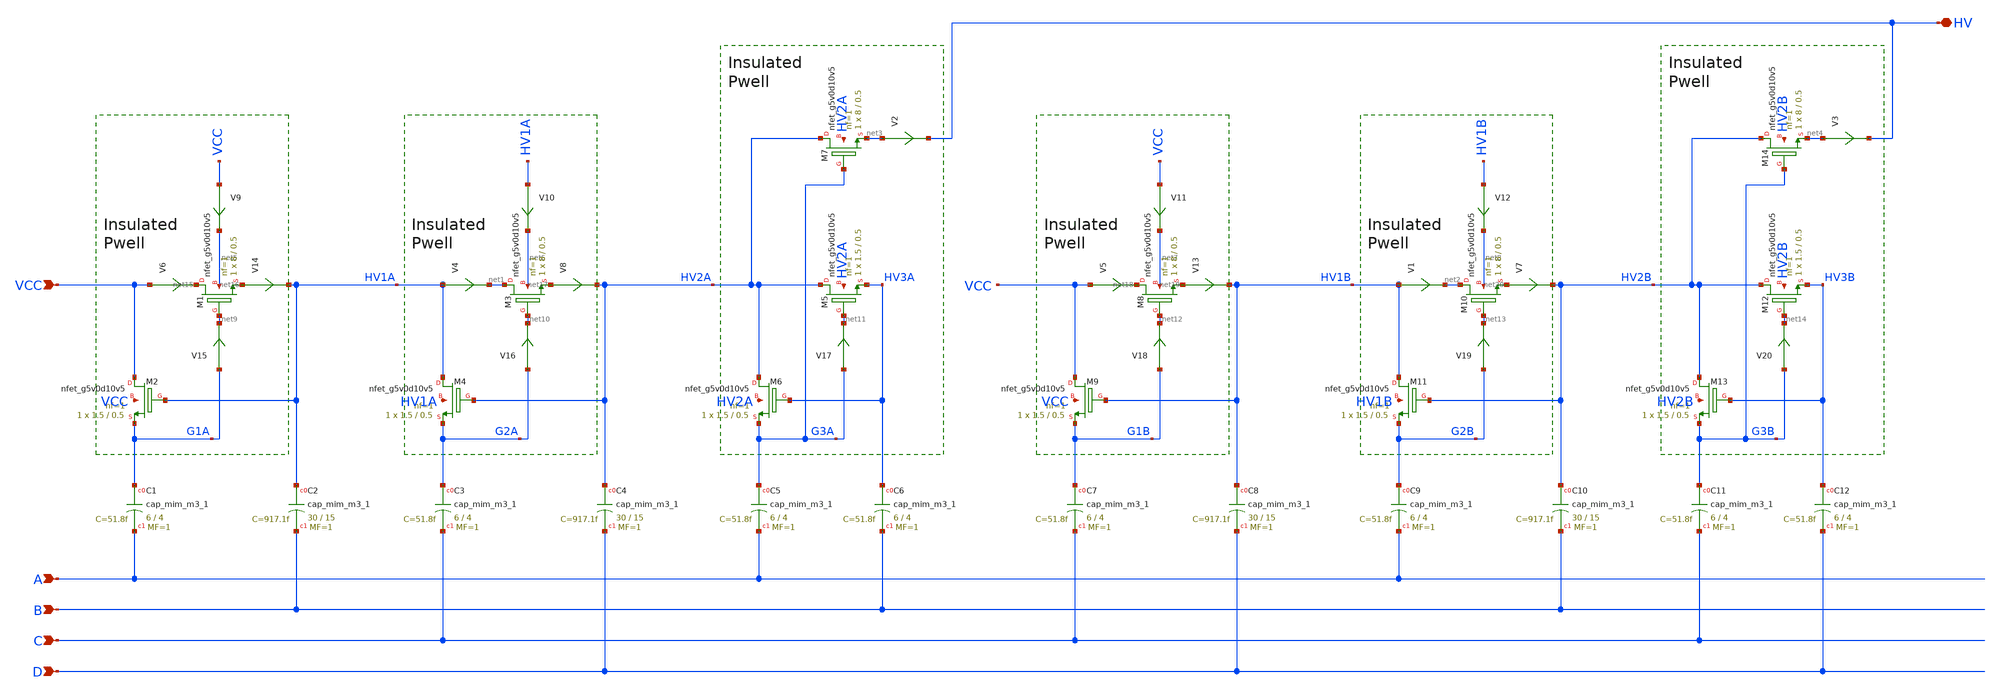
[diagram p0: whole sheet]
** sch_path: sky130A/xschem_libs/sky130_tests_ase/charge_pump/schematic/charge_pump.sch
* Copyright 2021 Stefan Frederik Schippers
* Licensed under the Apache License, Version 2.0 (the "License");
* you may not use this file except in compliance with the License.
* You may obtain a copy of the License at
* https://www.apache.org/licenses/LICENSE-2.0
* Unless required by applicable law or agreed to in writing, software
* distributed under the License is distributed on an "AS IS" BASIS,
* WITHOUT WARRANTIES OR CONDITIONS OF ANY KIND, either express or implied.
* See the License for the specific language governing permissions and
* limitations under the License.
**.subckt charge_pump A B C D VCC HV
*.ipin A
*.ipin B
*.ipin C
*.ipin D
*.ipin VCC
*.iopin HV
XM1 net15 net9 net16 net5 sky130_fd_pr__nfet_g5v0d10v5 L=0.5 W=8 nf=1 ad='int((1 + 1)/2) * 8 / 1 * 0.29'
+ as='int((1 + 2)/2) * 8 / 1 * 0.29' pd='2*int((1 + 1)/2) * (8 / 1 + 0.29)' ps='2*int((1 + 2)/2) * (8 / 1 + 0.29)'
+ nrd='0.29 / 8 ' nrs='0.29 / 8 ' sa=0 sb=0 sd=0 mult=1 m=1
XM2 VCC HV1A G1A VCC sky130_fd_pr__nfet_g5v0d10v5 L=0.5 W=1.5 nf=1 ad='int((1 + 1)/2) * 1.5 / 1 * 0.29'
+ as='int((1 + 2)/2) * 1.5 / 1 * 0.29' pd='2*int((1 + 1)/2) * (1.5 / 1 + 0.29)' ps='2*int((1 + 2)/2) * (1.5 / 1 + 0.29)'
+ nrd='0.29 / 1.5 ' nrs='0.29 / 1.5 ' sa=0 sb=0 sd=0 mult=1 m=1
XM3 net1 net10 net17 net6 sky130_fd_pr__nfet_g5v0d10v5 L=0.5 W=8 nf=1 ad='int((1 + 1)/2) * 8 / 1 * 0.29'
+ as='int((1 + 2)/2) * 8 / 1 * 0.29' pd='2*int((1 + 1)/2) * (8 / 1 + 0.29)' ps='2*int((1 + 2)/2) * (8 / 1 + 0.29)'
+ nrd='0.29 / 8 ' nrs='0.29 / 8 ' sa=0 sb=0 sd=0 mult=1 m=1
XM4 HV1A HV2A G2A HV1A sky130_fd_pr__nfet_g5v0d10v5 L=0.5 W=1.5 nf=1 ad='int((1 + 1)/2) * 1.5 / 1 * 0.29'
+ as='int((1 + 2)/2) * 1.5 / 1 * 0.29' pd='2*int((1 + 1)/2) * (1.5 / 1 + 0.29)' ps='2*int((1 + 2)/2) * (1.5 / 1 + 0.29)'
+ nrd='0.29 / 1.5 ' nrs='0.29 / 1.5 ' sa=0 sb=0 sd=0 mult=1 m=1
XM5 HV2A net11 HV3A HV2A sky130_fd_pr__nfet_g5v0d10v5 L=0.5 W=1.5 nf=1 ad='int((1 + 1)/2) * 1.5 / 1 * 0.29'
+ as='int((1 + 2)/2) * 1.5 / 1 * 0.29' pd='2*int((1 + 1)/2) * (1.5 / 1 + 0.29)' ps='2*int((1 + 2)/2) * (1.5 / 1 + 0.29)'
+ nrd='0.29 / 1.5 ' nrs='0.29 / 1.5 ' sa=0 sb=0 sd=0 mult=1 m=1
XM6 HV2A HV3A G3A HV2A sky130_fd_pr__nfet_g5v0d10v5 L=0.5 W=1.5 nf=1 ad='int((1 + 1)/2) * 1.5 / 1 * 0.29'
+ as='int((1 + 2)/2) * 1.5 / 1 * 0.29' pd='2*int((1 + 1)/2) * (1.5 / 1 + 0.29)' ps='2*int((1 + 2)/2) * (1.5 / 1 + 0.29)'
+ nrd='0.29 / 1.5 ' nrs='0.29 / 1.5 ' sa=0 sb=0 sd=0 mult=1 m=1
XM7 HV2A G3A net3 HV2A sky130_fd_pr__nfet_g5v0d10v5 L=0.5 W=8 nf=1 ad='int((1 + 1)/2) * 8 / 1 * 0.29'
+ as='int((1 + 2)/2) * 8 / 1 * 0.29' pd='2*int((1 + 1)/2) * (8 / 1 + 0.29)' ps='2*int((1 + 2)/2) * (8 / 1 + 0.29)'
+ nrd='0.29 / 8 ' nrs='0.29 / 8 ' sa=0 sb=0 sd=0 mult=1 m=1
XC1 G1A A sky130_fd_pr__cap_mim_m3_1 W=6 L=4 MF=1 m=1
XC2 HV1A B sky130_fd_pr__cap_mim_m3_1 W=30 L=15 MF=1 m=1
XC3 G2A C sky130_fd_pr__cap_mim_m3_1 W=6 L=4 MF=1 m=1
XC4 HV2A D sky130_fd_pr__cap_mim_m3_1 W=30 L=15 MF=1 m=1
XC5 G3A A sky130_fd_pr__cap_mim_m3_1 W=6 L=4 MF=1 m=1
XC6 HV3A B sky130_fd_pr__cap_mim_m3_1 W=6 L=4 MF=1 m=1
XM8 net18 net12 net19 net7 sky130_fd_pr__nfet_g5v0d10v5 L=0.5 W=8 nf=1 ad='int((1 + 1)/2) * 8 / 1 * 0.29'
+ as='int((1 + 2)/2) * 8 / 1 * 0.29' pd='2*int((1 + 1)/2) * (8 / 1 + 0.29)' ps='2*int((1 + 2)/2) * (8 / 1 + 0.29)'
+ nrd='0.29 / 8 ' nrs='0.29 / 8 ' sa=0 sb=0 sd=0 mult=1 m=1
XM9 VCC HV1B G1B VCC sky130_fd_pr__nfet_g5v0d10v5 L=0.5 W=1.5 nf=1 ad='int((1 + 1)/2) * 1.5 / 1 * 0.29'
+ as='int((1 + 2)/2) * 1.5 / 1 * 0.29' pd='2*int((1 + 1)/2) * (1.5 / 1 + 0.29)' ps='2*int((1 + 2)/2) * (1.5 / 1 + 0.29)'
+ nrd='0.29 / 1.5 ' nrs='0.29 / 1.5 ' sa=0 sb=0 sd=0 mult=1 m=1
XM10 net2 net13 net20 net8 sky130_fd_pr__nfet_g5v0d10v5 L=0.5 W=8 nf=1 ad='int((1 + 1)/2) * 8 / 1 * 0.29'
+ as='int((1 + 2)/2) * 8 / 1 * 0.29' pd='2*int((1 + 1)/2) * (8 / 1 + 0.29)' ps='2*int((1 + 2)/2) * (8 / 1 + 0.29)'
+ nrd='0.29 / 8 ' nrs='0.29 / 8 ' sa=0 sb=0 sd=0 mult=1 m=1
XM11 HV1B HV2B G2B HV1B sky130_fd_pr__nfet_g5v0d10v5 L=0.5 W=1.5 nf=1 ad='int((1 + 1)/2) * 1.5 / 1 * 0.29'
+ as='int((1 + 2)/2) * 1.5 / 1 * 0.29' pd='2*int((1 + 1)/2) * (1.5 / 1 + 0.29)' ps='2*int((1 + 2)/2) * (1.5 / 1 + 0.29)'
+ nrd='0.29 / 1.5 ' nrs='0.29 / 1.5 ' sa=0 sb=0 sd=0 mult=1 m=1
XM12 HV2B net14 HV3B HV2B sky130_fd_pr__nfet_g5v0d10v5 L=0.5 W=1.5 nf=1 ad='int((1 + 1)/2) * 1.5 / 1 * 0.29'
+ as='int((1 + 2)/2) * 1.5 / 1 * 0.29' pd='2*int((1 + 1)/2) * (1.5 / 1 + 0.29)' ps='2*int((1 + 2)/2) * (1.5 / 1 + 0.29)'
+ nrd='0.29 / 1.5 ' nrs='0.29 / 1.5 ' sa=0 sb=0 sd=0 mult=1 m=1
XM13 HV2B HV3B G3B HV2B sky130_fd_pr__nfet_g5v0d10v5 L=0.5 W=1.5 nf=1 ad='int((1 + 1)/2) * 1.5 / 1 * 0.29'
+ as='int((1 + 2)/2) * 1.5 / 1 * 0.29' pd='2*int((1 + 1)/2) * (1.5 / 1 + 0.29)' ps='2*int((1 + 2)/2) * (1.5 / 1 + 0.29)'
+ nrd='0.29 / 1.5 ' nrs='0.29 / 1.5 ' sa=0 sb=0 sd=0 mult=1 m=1
XM14 HV2B G3B net4 HV2B sky130_fd_pr__nfet_g5v0d10v5 L=0.5 W=8 nf=1 ad='int((1 + 1)/2) * 8 / 1 * 0.29'
+ as='int((1 + 2)/2) * 8 / 1 * 0.29' pd='2*int((1 + 1)/2) * (8 / 1 + 0.29)' ps='2*int((1 + 2)/2) * (8 / 1 + 0.29)'
+ nrd='0.29 / 8 ' nrs='0.29 / 8 ' sa=0 sb=0 sd=0 mult=1 m=1
XC7 G1B C sky130_fd_pr__cap_mim_m3_1 W=6 L=4 MF=1 m=1
XC8 HV1B D sky130_fd_pr__cap_mim_m3_1 W=30 L=15 MF=1 m=1
XC9 G2B A sky130_fd_pr__cap_mim_m3_1 W=6 L=4 MF=1 m=1
XC10 HV2B B sky130_fd_pr__cap_mim_m3_1 W=30 L=15 MF=1 m=1
XC11 G3B C sky130_fd_pr__cap_mim_m3_1 W=6 L=4 MF=1 m=1
XC12 HV3B D sky130_fd_pr__cap_mim_m3_1 W=6 L=4 MF=1 m=1
V1 HV1B net2 0
.save i(v1)
V2 net3 HV 0
.save i(v2)
V3 net4 HV 0
.save i(v3)
V4 HV1A net1 0
.save i(v4)
V5 VCC net18 0
.save i(v5)
V6 VCC net15 0
.save i(v6)
V7 net20 HV2B 0
.save i(v7)
V8 net17 HV2A 0
.save i(v8)
V9 VCC net5 0
.save i(v9)
V10 HV1A net6 0
.save i(v10)
V11 VCC net7 0
.save i(v11)
V12 HV1B net8 0
.save i(v12)
V13 net19 HV1B 0
.save i(v13)
V14 net16 HV1A 0
.save i(v14)
V15 G1A net9 0
.save i(v15)
V16 G2A net10 0
.save i(v16)
V17 G3A net11 0
.save i(v17)
V18 G1B net12 0
.save i(v18)
V19 G2B net13 0
.save i(v19)
V20 G3B net14 0
.save i(v20)
**.ends
.end
